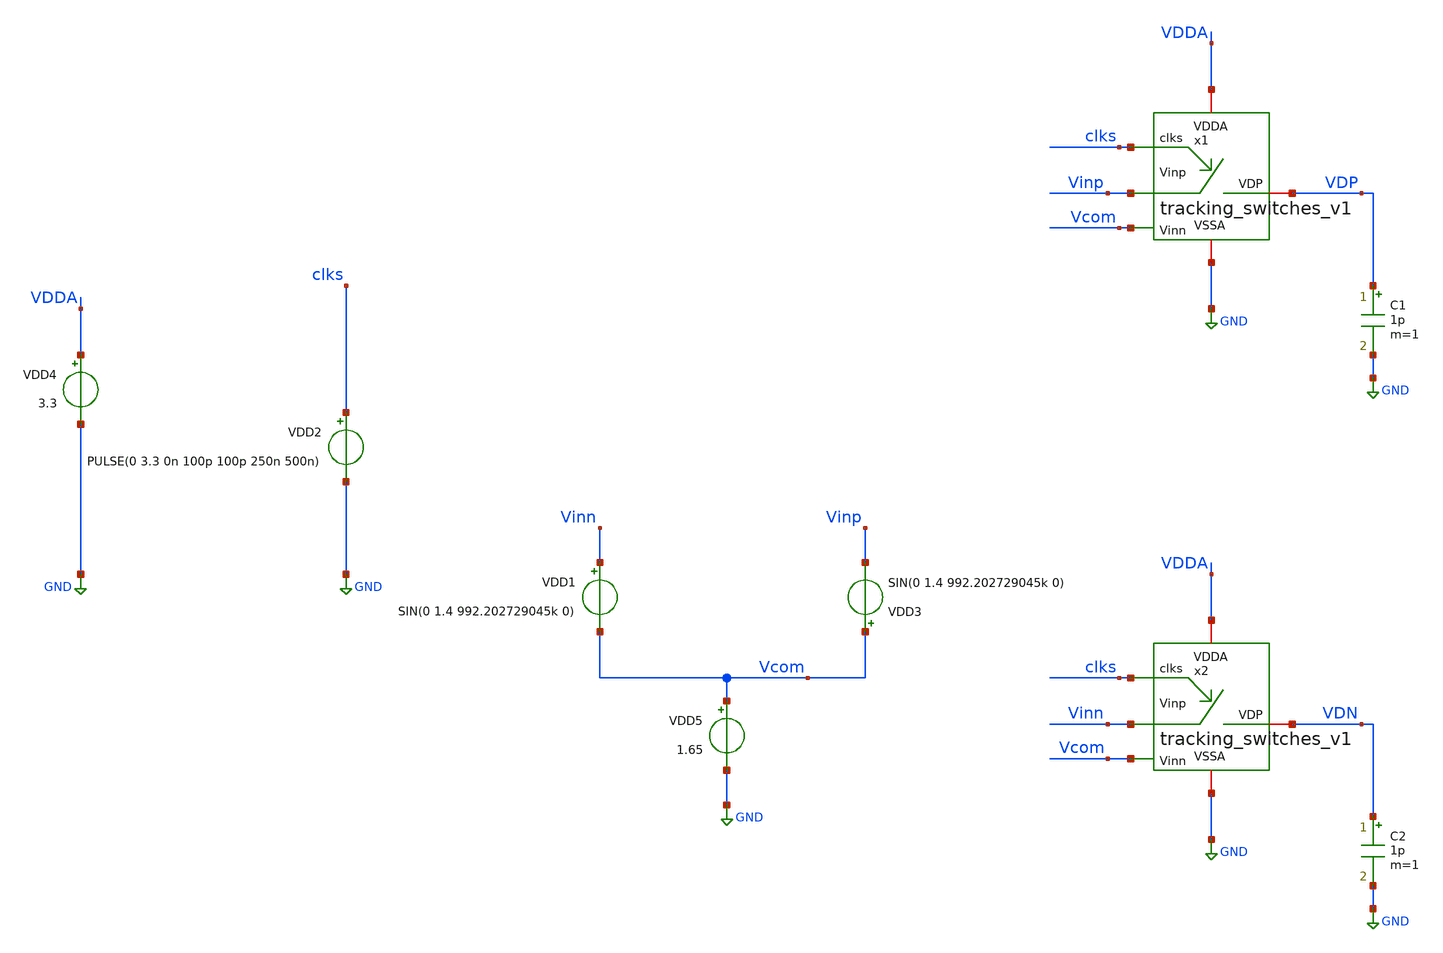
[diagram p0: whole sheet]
** sch_path: SAR_ADC/tracking_switches/xschem/tracking_switches_tb.sch
**.subckt tracking_switches_tb
x1 VDP VDDA GND clks Vinp Vcom tracking_switches_v1
VDD2 clks GND PULSE(0 3.3 0n 100p 100p 250n 500n)
VDD4 VDDA GND 3.3
x2 VDN VDDA GND clks Vinn Vcom tracking_switches_v1
VDD1 Vinn Vcom SIN(0 1.4 992.202729045k 0)
VDD3 Vcom Vinp SIN(0 1.4 992.202729045k 0)
VDD5 Vcom GND 1.65
C1 VDP GND 1p m=1
C2 VDN GND 1p m=1
**** begin user architecture code



*Parameters

.options TEMP = 50.0
.lib /home/gf180/Documents/gf180/pdk/gf180mcuD/libs.tech/ngspice/sm141064.ngspice typical
.include /home/gf180/Documents/gf180/pdk/gf180mcuD/libs.tech/ngspice/design.ngspice
.lib /home/gf180/Documents/gf180/pdk/gf180mcuD/libs.tech/ngspice/sm141064.ngspice cap_mim
.lib /home/gf180/Documents/gf180/pdk/gf180mcuD/libs.tech/ngspice/sm141064.ngspice mimcap_statistical

*Data to save
*.save all
.save V(VDP)
.save V(VDN)
.save V(Vinp)
.save V(Vinn)
.save V(vin_diff)
.save V(vout_diff)
.save V(clks)

* Simulation
.control
tran 10n 513u
.option method=gear reltol=1e-6 interp
*.options output initial_interval=500e-9
*setplot dc1
*let Vgs_xm1 = V(.x1.VG_XM1) - V(.x1.VS_XM1)
*let Vds_xm1 = V(.x1.VS_XM1) - V(Vinp)
*plot Vgs_xm1 Vds_xm1

*setplot dc2
*let Vgs_xm2 = V(.x1.n_clkc)
*let Vds_xm2 = V(.x1.VS_XM1)
*plot Vgs_xm2 Vds_xm2

*setplot dc3
*let Vgs_xm3 = V(.x1.VG_XM1) - V(.x1.VS_XM1)
*let Vds_xm3 = V(.x1.VD_XM5) - V(.x1.VS_XM1)
*plot Vgs_xm3 Vds_xm3

*setplot dc4
*let Vgs_xm4 = V(clks) - V(.x1.VS_XM1)
*let Vds_xm4 = V(.x1.VD_XM5) - V(.x1.VS_XM1)
*plot Vgs_xm4 Vds_xm4

*setplot dc5
*let Vsg_xm5 = V(VDDA) - V(clks)
*let vsd_xm5 = V(VDDA) - V(.x1.VD_XM5)
*plot Vsg_xm5 vsd_xm5

*setplot dc6
*let Vsg_xm6 = V(VDDA) - V(.x1.VG_XM1)
*let vsd_xm6 = V(VDDA) - V(.x1.VS_XM6)
*plot Vsg_xm6 vsd_xm6

*setplot dc7
*let Vsg_xm7 = V(.x1.VS_XM6) - V(.x1.VD_XM5)
*let vsd_xm7 = V(.x1.VS_XM6) - V(.x1.VG_XM1)
*plot Vsg_xm7 vsd_xm7

*setplot dc8
*let Vsg_xm8 = V(VDDA) - V(.x1.VS_XM8)
*let vsd_xm8 = V(.x1.VG_XM1) - V(.x1.VS_XM8)
*plot Vsg_xm8 vsd_xm8

*setplot dc9
*let Vsg_xm9 = V(.x1.n_clkc)
*let vsd_xm9 = V(.x1.VS_XM8)
*plot Vsg_xm9 vsd_xm9

setplot dc1
let vout_diff= V(VDP) - V(VDN)
let vin_diff= V(Vinp)-V(Vinn)
*plot V(clks)+8 V(Vinp)+4 V(Vinn) V(VDP)+4 V(VDN)
plot vin_diff vout_diff

wrdata output.txt clks vin_diff vout_diff
*set filetype = ascii
*write tracking_switches_tb_tran.raw

reset
unset filetype
op
save all
*write tracking_switches_tb.raw


.endc
.end


**** end user architecture code
**.ends

* expanding   symbol:  PICO_contest/tracking_switches/xschem/tracking_switches_v1.sym # of pins=6
** sym_path: SAR_ADC/tracking_switches/xschem/tracking_switches_v1.sym
** sch_path: SAR_ADC/tracking_switches/xschem/tracking_switches_v1.sch
.subckt tracking_switches_v1 VDP VDDA VSSA clks Vinp Vinn
*.iopin VDDA
*.iopin VSSA
*.ipin clks
*.ipin Vinp
*.iopin VDP
*.ipin Vinn
XM2 VS_XM1 n_clks VSSA VSSA nfet_03v3 L=0.28u W=1.56u nf=1 ad='int((nf+1)/2) * W/nf * 0.18u' as='int((nf+2)/2) * W/nf * 0.18u'
+ pd='2*int((nf+1)/2) * (W/nf + 0.18u)' ps='2*int((nf+2)/2) * (W/nf + 0.18u)' nrd='0.18u / W' nrs='0.18u / W'
+ sa=0 sb=0 sd=0 m=1
XM4 VD_XM5 clks_in VS_XM1 VSSA nfet_03v3 L=0.28u W=1.56u nf=1 ad='int((nf+1)/2) * W/nf * 0.18u' as='int((nf+2)/2) * W/nf * 0.18u'
+ pd='2*int((nf+1)/2) * (W/nf + 0.18u)' ps='2*int((nf+2)/2) * (W/nf + 0.18u)' nrd='0.18u / W' nrs='0.18u / W'
+ sa=0 sb=0 sd=0 m=1
XM3 VD_XM5 VG_XM1 VS_XM1 VSSA nfet_03v3 L=0.28u W=1.56u nf=1 ad='int((nf+1)/2) * W/nf * 0.18u' as='int((nf+2)/2) * W/nf * 0.18u'
+ pd='2*int((nf+1)/2) * (W/nf + 0.18u)' ps='2*int((nf+2)/2) * (W/nf + 0.18u)' nrd='0.18u / W' nrs='0.18u / W'
+ sa=0 sb=0 sd=0 m=1
XM5 VD_XM5 clks_in VDDA VDDA pfet_03v3 L=0.28u W=3.9u nf=1 ad='int((nf+1)/2) * W/nf * 0.18u' as='int((nf+2)/2) * W/nf * 0.18u'
+ pd='2*int((nf+1)/2) * (W/nf + 0.18u)' ps='2*int((nf+2)/2) * (W/nf + 0.18u)' nrd='0.18u / W' nrs='0.18u / W'
+ sa=0 sb=0 sd=0 m=1
XM6 VDDA VG_XM1 VS_XM6 VS_XM6 pfet_03v3 L=0.28u W=3.9u nf=1 ad='int((nf+1)/2) * W/nf * 0.18u' as='int((nf+2)/2) * W/nf * 0.18u'
+ pd='2*int((nf+1)/2) * (W/nf + 0.18u)' ps='2*int((nf+2)/2) * (W/nf + 0.18u)' nrd='0.18u / W' nrs='0.18u / W'
+ sa=0 sb=0 sd=0 m=1
XM7 VG_XM1 VD_XM5 VS_XM6 VS_XM6 pfet_03v3 L=0.28u W=3.9u nf=1 ad='int((nf+1)/2) * W/nf * 0.18u' as='int((nf+2)/2) * W/nf * 0.18u'
+ pd='2*int((nf+1)/2) * (W/nf + 0.18u)' ps='2*int((nf+2)/2) * (W/nf + 0.18u)' nrd='0.18u / W' nrs='0.18u / W'
+ sa=0 sb=0 sd=0 m=1
XM1 Vinp VG_XM1 VS_XM1 VSSA nfet_03v3 L=0.28u W=1.56u nf=1 ad='int((nf+1)/2) * W/nf * 0.18u' as='int((nf+2)/2) * W/nf * 0.18u'
+ pd='2*int((nf+1)/2) * (W/nf + 0.18u)' ps='2*int((nf+2)/2) * (W/nf + 0.18u)' nrd='0.18u / W' nrs='0.18u / W'
+ sa=0 sb=0 sd=0 m=1
XM9 VS_XM8 n_clks VSSA VSSA nfet_03v3 L=0.28u W=1.56u nf=1 ad='int((nf+1)/2) * W/nf * 0.18u' as='int((nf+2)/2) * W/nf * 0.18u'
+ pd='2*int((nf+1)/2) * (W/nf + 0.18u)' ps='2*int((nf+2)/2) * (W/nf + 0.18u)' nrd='0.18u / W' nrs='0.18u / W'
+ sa=0 sb=0 sd=0 m=1
XM8 VG_XM1 VDDA VS_XM8 VSSA nfet_03v3 L=0.28u W=1.56u nf=1 ad='int((nf+1)/2) * W/nf * 0.18u' as='int((nf+2)/2) * W/nf * 0.18u'
+ pd='2*int((nf+1)/2) * (W/nf + 0.18u)' ps='2*int((nf+2)/2) * (W/nf + 0.18u)' nrd='0.18u / W' nrs='0.18u / W'
+ sa=0 sb=0 sd=0 m=1
x1 VDDA VSSA n_clks clks tracking_switches_inv_1x
x2 VDDA VSSA clks_in n_clks tracking_switches_inv_1x
XMS2 VDP VG_XM1 Vinp VSSA nfet_03v3 L=0.28u W=30u nf=1 ad='int((nf+1)/2) * W/nf * 0.18u' as='int((nf+2)/2) * W/nf * 0.18u'
+ pd='2*int((nf+1)/2) * (W/nf + 0.18u)' ps='2*int((nf+2)/2) * (W/nf + 0.18u)' nrd='0.18u / W' nrs='0.18u / W'
+ sa=0 sb=0 sd=0 m=1
XC12[1] VS_XM6 VS_XM1 cap_mim_2f0_m4m5_noshield c_width=10e-6 c_length=10e-6 m=1
XC12[2] VS_XM6 VS_XM1 cap_mim_2f0_m4m5_noshield c_width=10e-6 c_length=10e-6 m=1
XC12[3] VS_XM6 VS_XM1 cap_mim_2f0_m4m5_noshield c_width=10e-6 c_length=10e-6 m=1
XMS1 VDP VSSA Vinn VSSA nfet_03v3 L=0.28u W=30u nf=1 ad='int((nf+1)/2) * W/nf * 0.18u' as='int((nf+2)/2) * W/nf * 0.18u'
+ pd='2*int((nf+1)/2) * (W/nf + 0.18u)' ps='2*int((nf+2)/2) * (W/nf + 0.18u)' nrd='0.18u / W' nrs='0.18u / W'
+ sa=0 sb=0 sd=0 m=1
.ends


* expanding   symbol:  PICO_contest/tracking_switches/xschem/tracking_switches_inv_1x.sym # of
*+ pins=4
** sym_path: SAR_ADC/blocks/tracking_switches/tracking_switches_inv_1x.sym
** sch_path: SAR_ADC/blocks/tracking_switches/tracking_switches_inv_1x.sch
.subckt tracking_switches_inv_1x VDDA VSSA OUT IN
*.iopin VDDA
*.iopin VSSA
*.iopin OUT
*.ipin IN
XM1 OUT IN VSSA VSSA nfet_03v3 L=0.28u W=0.22u nf=1 ad='int((nf+1)/2) * W/nf * 0.18u' as='int((nf+2)/2) * W/nf * 0.18u'
+ pd='2*int((nf+1)/2) * (W/nf + 0.18u)' ps='2*int((nf+2)/2) * (W/nf + 0.18u)' nrd='0.18u / W' nrs='0.18u / W'
+ sa=0 sb=0 sd=0 m=1
XM2 OUT IN VDDA VDDA pfet_03v3 L=0.28u W=0.66u nf=1 ad='int((nf+1)/2) * W/nf * 0.18u' as='int((nf+2)/2) * W/nf * 0.18u'
+ pd='2*int((nf+1)/2) * (W/nf + 0.18u)' ps='2*int((nf+2)/2) * (W/nf + 0.18u)' nrd='0.18u / W' nrs='0.18u / W'
+ sa=0 sb=0 sd=0 m=1
.ends

.GLOBAL GND
.end
